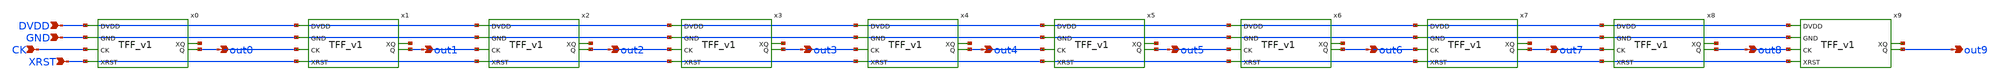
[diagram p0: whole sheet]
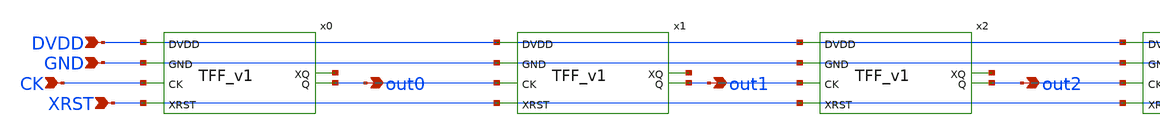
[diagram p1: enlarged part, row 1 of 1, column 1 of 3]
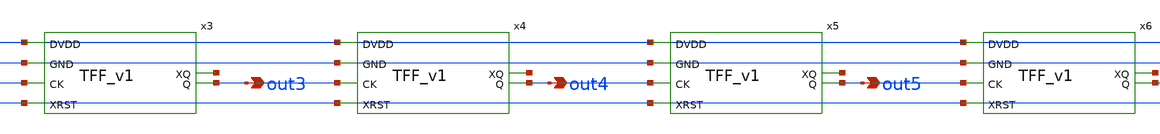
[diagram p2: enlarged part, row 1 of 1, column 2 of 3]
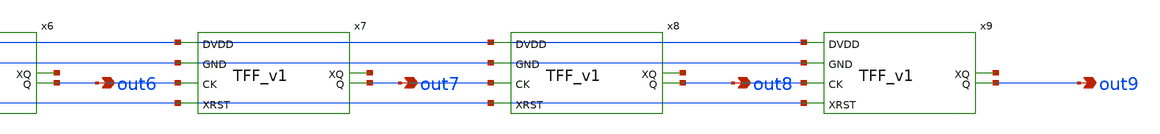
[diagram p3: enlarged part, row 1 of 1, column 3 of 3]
** sch_path: design/schematic/RC10b_v1.sch
**.subckt RC10b_v1 CK XRST DVDD GND out9 out7 out8 out6 out5 out4 out3 out2 out1 out0
*.ipin CK
*.ipin XRST
*.ipin DVDD
*.ipin GND
*.opin out9
*.opin out7
*.opin out8
*.opin out6
*.opin out5
*.opin out4
*.opin out3
*.opin out2
*.opin out1
*.opin out0
x0 DVDD GND net1 out0 CK XRST TFF_v1
x1 DVDD GND net2 out1 out0 XRST TFF_v1
x2 DVDD GND net3 out2 out1 XRST TFF_v1
x3 DVDD GND net4 out3 out2 XRST TFF_v1
x4 DVDD GND net5 out4 out3 XRST TFF_v1
x5 DVDD GND net6 out5 out4 XRST TFF_v1
x6 DVDD GND net7 out6 out5 XRST TFF_v1
x7 DVDD GND net8 out7 out6 XRST TFF_v1
x8 DVDD GND net9 out8 out7 XRST TFF_v1
x9 DVDD GND net10 out9 out8 XRST TFF_v1
**.ends

* expanding   symbol:  /home/ttuser/TT_WORK/rel/TFF_v1.sym # of pins=6
** sym_path: design/schematic/TFF_v1.sym
** sch_path: design/schematic/TFF_v1.sch
.subckt TFF_v1 DVDD GND XQ Q CK XRST
*.ipin CK
*.ipin XRST
*.opin XQ
*.opin Q
*.ipin DVDD
*.ipin GND
x0 CK XQ XRST GND GND DVDD DVDD Q XQ sky130_fd_sc_hd__dfrbp_1
.ends

.end
